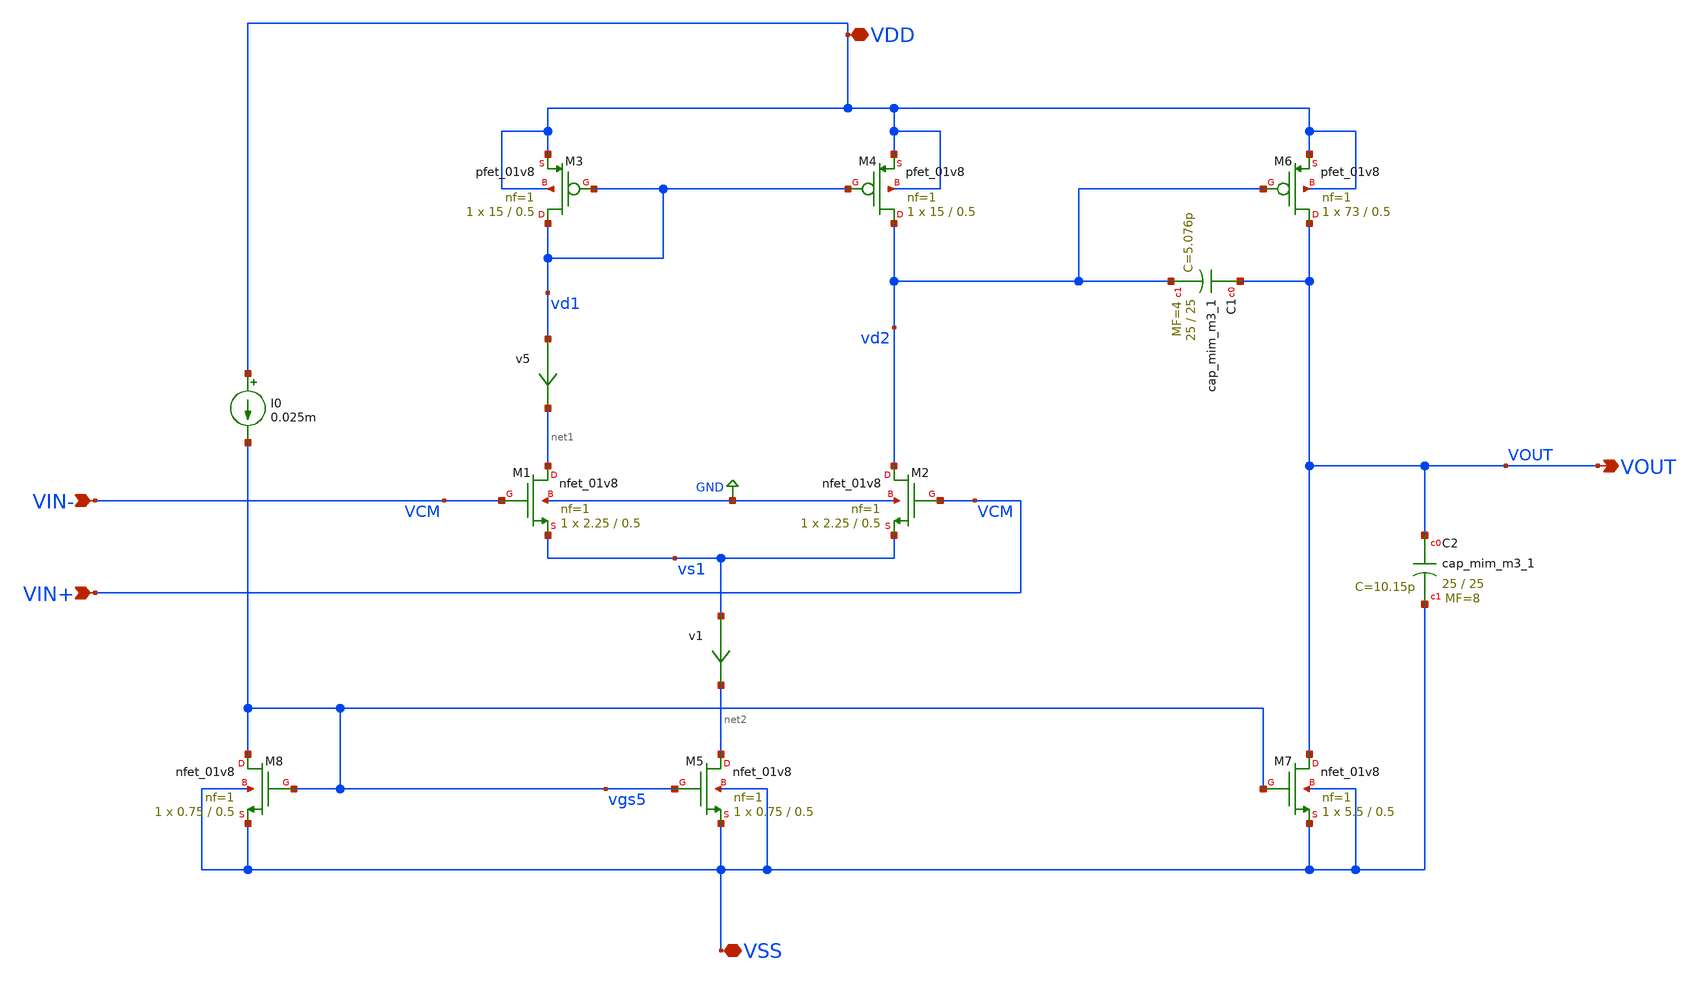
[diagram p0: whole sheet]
** sch_path: xschem/untitled-1.sch
**.subckt untitled-1 VIN+ VOUT VSS VDD VIN-
*.ipin VIN+
*.opin VOUT
*.iopin VSS
*.iopin VDD
*.ipin VIN-
XM1 net1 VCM vs1 GND sky130_fd_pr__nfet_01v8 L=0.5 W=2.25 nf=1 ad='int((nf+1)/2) * W/nf * 0.29' as='int((nf+2)/2) * W/nf * 0.29'
+ pd='2*int((nf+1)/2) * (W/nf + 0.29)' ps='2*int((nf+2)/2) * (W/nf + 0.29)' nrd='0.29 / W' nrs='0.29 / W'
+ sa=0 sb=0 sd=0 mult=1 m=1
XM2 vd2 VCM vs1 GND sky130_fd_pr__nfet_01v8 L=0.5 W=2.25 nf=1 ad='int((nf+1)/2) * W/nf * 0.29' as='int((nf+2)/2) * W/nf * 0.29'
+ pd='2*int((nf+1)/2) * (W/nf + 0.29)' ps='2*int((nf+2)/2) * (W/nf + 0.29)' nrd='0.29 / W' nrs='0.29 / W'
+ sa=0 sb=0 sd=0 mult=1 m=1
XM3 vd1 vd1 VDD VDD sky130_fd_pr__pfet_01v8 L=0.5 W=15 nf=1 ad='int((nf+1)/2) * W/nf * 0.29' as='int((nf+2)/2) * W/nf * 0.29'
+ pd='2*int((nf+1)/2) * (W/nf + 0.29)' ps='2*int((nf+2)/2) * (W/nf + 0.29)' nrd='0.29 / W' nrs='0.29 / W'
+ sa=0 sb=0 sd=0 mult=1 m=1
XM4 vd2 vd1 VDD VDD sky130_fd_pr__pfet_01v8 L=0.5 W=15 nf=1 ad='int((nf+1)/2) * W/nf * 0.29' as='int((nf+2)/2) * W/nf * 0.29'
+ pd='2*int((nf+1)/2) * (W/nf + 0.29)' ps='2*int((nf+2)/2) * (W/nf + 0.29)' nrd='0.29 / W' nrs='0.29 / W'
+ sa=0 sb=0 sd=0 mult=1 m=1
XM5 net2 vgs5 VSS VSS sky130_fd_pr__nfet_01v8 L=0.5 W=0.75 nf=1 ad='int((nf+1)/2) * W/nf * 0.29' as='int((nf+2)/2) * W/nf * 0.29'
+ pd='2*int((nf+1)/2) * (W/nf + 0.29)' ps='2*int((nf+2)/2) * (W/nf + 0.29)' nrd='0.29 / W' nrs='0.29 / W'
+ sa=0 sb=0 sd=0 mult=1 m=1
XM6 VOUT vd2 VDD VDD sky130_fd_pr__pfet_01v8 L=0.5 W=73 nf=1 ad='int((nf+1)/2) * W/nf * 0.29' as='int((nf+2)/2) * W/nf * 0.29'
+ pd='2*int((nf+1)/2) * (W/nf + 0.29)' ps='2*int((nf+2)/2) * (W/nf + 0.29)' nrd='0.29 / W' nrs='0.29 / W'
+ sa=0 sb=0 sd=0 mult=1 m=1
XM7 VOUT vgs5 VSS VSS sky130_fd_pr__nfet_01v8 L=0.5 W=5.5 nf=1 ad='int((nf+1)/2) * W/nf * 0.29' as='int((nf+2)/2) * W/nf * 0.29'
+ pd='2*int((nf+1)/2) * (W/nf + 0.29)' ps='2*int((nf+2)/2) * (W/nf + 0.29)' nrd='0.29 / W' nrs='0.29 / W'
+ sa=0 sb=0 sd=0 mult=1 m=1
XM8 vgs5 vgs5 VSS VSS sky130_fd_pr__nfet_01v8 L=0.5 W=0.75 nf=1 ad='int((nf+1)/2) * W/nf * 0.29' as='int((nf+2)/2) * W/nf * 0.29'
+ pd='2*int((nf+1)/2) * (W/nf + 0.29)' ps='2*int((nf+2)/2) * (W/nf + 0.29)' nrd='0.29 / W' nrs='0.29 / W'
+ sa=0 sb=0 sd=0 mult=1 m=1
XC1 VOUT vd2 sky130_fd_pr__cap_mim_m3_1 W=25 L=25 MF=4 m=4
XC2 VOUT VSS sky130_fd_pr__cap_mim_m3_1 W=25 L=25 MF=8 m=8
I0 VDD vgs5 0.025m
v5 vd1 net1 0
.save i(v5)
v1 vs1 net2 0
.save i(v1)
**.ends
.GLOBAL GND
.end
